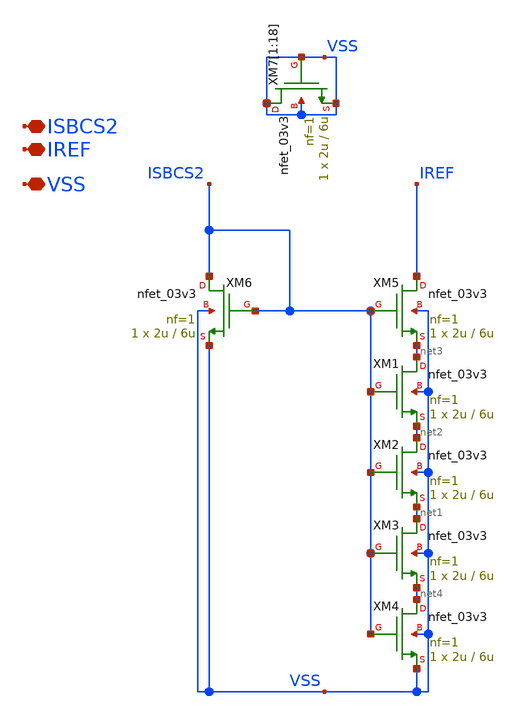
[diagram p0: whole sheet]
** sch_path: TIA_Filter/CurrentMirrors/CM_iref.sch
**.subckt CM_iref ISBCS2 IREF VSS
*.iopin ISBCS2
*.iopin IREF
*.iopin VSS
XM6 ISBCS2 ISBCS2 VSS VSS nfet_03v3 L=6u W=2u nf=1 ad='int((nf+1)/2) * W/nf * 0.18u' as='int((nf+2)/2) * W/nf * 0.18u'
+ pd='2*int((nf+1)/2) * (W/nf + 0.18u)' ps='2*int((nf+2)/2) * (W/nf + 0.18u)' nrd='0.18u / W' nrs='0.18u / W'
+ sa=0 sb=0 sd=0 m=1
XM5 IREF ISBCS2 net3 VSS nfet_03v3 L=6u W=2u nf=1 ad='int((nf+1)/2) * W/nf * 0.18u' as='int((nf+2)/2) * W/nf * 0.18u'
+ pd='2*int((nf+1)/2) * (W/nf + 0.18u)' ps='2*int((nf+2)/2) * (W/nf + 0.18u)' nrd='0.18u / W' nrs='0.18u / W'
+ sa=0 sb=0 sd=0 m=1
XM1 net3 ISBCS2 net2 VSS nfet_03v3 L=6u W=2u nf=1 ad='int((nf+1)/2) * W/nf * 0.18u' as='int((nf+2)/2) * W/nf * 0.18u'
+ pd='2*int((nf+1)/2) * (W/nf + 0.18u)' ps='2*int((nf+2)/2) * (W/nf + 0.18u)' nrd='0.18u / W' nrs='0.18u / W'
+ sa=0 sb=0 sd=0 m=1
XM2 net2 ISBCS2 net1 VSS nfet_03v3 L=6u W=2u nf=1 ad='int((nf+1)/2) * W/nf * 0.18u' as='int((nf+2)/2) * W/nf * 0.18u'
+ pd='2*int((nf+1)/2) * (W/nf + 0.18u)' ps='2*int((nf+2)/2) * (W/nf + 0.18u)' nrd='0.18u / W' nrs='0.18u / W'
+ sa=0 sb=0 sd=0 m=1
XM3 net1 ISBCS2 net4 VSS nfet_03v3 L=6u W=2u nf=1 ad='int((nf+1)/2) * W/nf * 0.18u' as='int((nf+2)/2) * W/nf * 0.18u'
+ pd='2*int((nf+1)/2) * (W/nf + 0.18u)' ps='2*int((nf+2)/2) * (W/nf + 0.18u)' nrd='0.18u / W' nrs='0.18u / W'
+ sa=0 sb=0 sd=0 m=1
XM4 net4 ISBCS2 VSS VSS nfet_03v3 L=6u W=2u nf=1 ad='int((nf+1)/2) * W/nf * 0.18u' as='int((nf+2)/2) * W/nf * 0.18u'
+ pd='2*int((nf+1)/2) * (W/nf + 0.18u)' ps='2*int((nf+2)/2) * (W/nf + 0.18u)' nrd='0.18u / W' nrs='0.18u / W'
+ sa=0 sb=0 sd=0 m=1
XM7[1] VSS VSS VSS VSS nfet_03v3 L=6u W=2u nf=1 ad='int((nf+1)/2) * W/nf * 0.18u' as='int((nf+2)/2) * W/nf * 0.18u'
+ pd='2*int((nf+1)/2) * (W/nf + 0.18u)' ps='2*int((nf+2)/2) * (W/nf + 0.18u)' nrd='0.18u / W' nrs='0.18u / W'
+ sa=0 sb=0 sd=0 m=1
XM7[2] VSS VSS VSS VSS nfet_03v3 L=6u W=2u nf=1 ad='int((nf+1)/2) * W/nf * 0.18u' as='int((nf+2)/2) * W/nf * 0.18u'
+ pd='2*int((nf+1)/2) * (W/nf + 0.18u)' ps='2*int((nf+2)/2) * (W/nf + 0.18u)' nrd='0.18u / W' nrs='0.18u / W'
+ sa=0 sb=0 sd=0 m=1
XM7[3] VSS VSS VSS VSS nfet_03v3 L=6u W=2u nf=1 ad='int((nf+1)/2) * W/nf * 0.18u' as='int((nf+2)/2) * W/nf * 0.18u'
+ pd='2*int((nf+1)/2) * (W/nf + 0.18u)' ps='2*int((nf+2)/2) * (W/nf + 0.18u)' nrd='0.18u / W' nrs='0.18u / W'
+ sa=0 sb=0 sd=0 m=1
XM7[4] VSS VSS VSS VSS nfet_03v3 L=6u W=2u nf=1 ad='int((nf+1)/2) * W/nf * 0.18u' as='int((nf+2)/2) * W/nf * 0.18u'
+ pd='2*int((nf+1)/2) * (W/nf + 0.18u)' ps='2*int((nf+2)/2) * (W/nf + 0.18u)' nrd='0.18u / W' nrs='0.18u / W'
+ sa=0 sb=0 sd=0 m=1
XM7[5] VSS VSS VSS VSS nfet_03v3 L=6u W=2u nf=1 ad='int((nf+1)/2) * W/nf * 0.18u' as='int((nf+2)/2) * W/nf * 0.18u'
+ pd='2*int((nf+1)/2) * (W/nf + 0.18u)' ps='2*int((nf+2)/2) * (W/nf + 0.18u)' nrd='0.18u / W' nrs='0.18u / W'
+ sa=0 sb=0 sd=0 m=1
XM7[6] VSS VSS VSS VSS nfet_03v3 L=6u W=2u nf=1 ad='int((nf+1)/2) * W/nf * 0.18u' as='int((nf+2)/2) * W/nf * 0.18u'
+ pd='2*int((nf+1)/2) * (W/nf + 0.18u)' ps='2*int((nf+2)/2) * (W/nf + 0.18u)' nrd='0.18u / W' nrs='0.18u / W'
+ sa=0 sb=0 sd=0 m=1
XM7[7] VSS VSS VSS VSS nfet_03v3 L=6u W=2u nf=1 ad='int((nf+1)/2) * W/nf * 0.18u' as='int((nf+2)/2) * W/nf * 0.18u'
+ pd='2*int((nf+1)/2) * (W/nf + 0.18u)' ps='2*int((nf+2)/2) * (W/nf + 0.18u)' nrd='0.18u / W' nrs='0.18u / W'
+ sa=0 sb=0 sd=0 m=1
XM7[8] VSS VSS VSS VSS nfet_03v3 L=6u W=2u nf=1 ad='int((nf+1)/2) * W/nf * 0.18u' as='int((nf+2)/2) * W/nf * 0.18u'
+ pd='2*int((nf+1)/2) * (W/nf + 0.18u)' ps='2*int((nf+2)/2) * (W/nf + 0.18u)' nrd='0.18u / W' nrs='0.18u / W'
+ sa=0 sb=0 sd=0 m=1
XM7[9] VSS VSS VSS VSS nfet_03v3 L=6u W=2u nf=1 ad='int((nf+1)/2) * W/nf * 0.18u' as='int((nf+2)/2) * W/nf * 0.18u'
+ pd='2*int((nf+1)/2) * (W/nf + 0.18u)' ps='2*int((nf+2)/2) * (W/nf + 0.18u)' nrd='0.18u / W' nrs='0.18u / W'
+ sa=0 sb=0 sd=0 m=1
XM7[10] VSS VSS VSS VSS nfet_03v3 L=6u W=2u nf=1 ad='int((nf+1)/2) * W/nf * 0.18u' as='int((nf+2)/2) * W/nf * 0.18u'
+ pd='2*int((nf+1)/2) * (W/nf + 0.18u)' ps='2*int((nf+2)/2) * (W/nf + 0.18u)' nrd='0.18u / W' nrs='0.18u / W'
+ sa=0 sb=0 sd=0 m=1
XM7[11] VSS VSS VSS VSS nfet_03v3 L=6u W=2u nf=1 ad='int((nf+1)/2) * W/nf * 0.18u' as='int((nf+2)/2) * W/nf * 0.18u'
+ pd='2*int((nf+1)/2) * (W/nf + 0.18u)' ps='2*int((nf+2)/2) * (W/nf + 0.18u)' nrd='0.18u / W' nrs='0.18u / W'
+ sa=0 sb=0 sd=0 m=1
XM7[12] VSS VSS VSS VSS nfet_03v3 L=6u W=2u nf=1 ad='int((nf+1)/2) * W/nf * 0.18u' as='int((nf+2)/2) * W/nf * 0.18u'
+ pd='2*int((nf+1)/2) * (W/nf + 0.18u)' ps='2*int((nf+2)/2) * (W/nf + 0.18u)' nrd='0.18u / W' nrs='0.18u / W'
+ sa=0 sb=0 sd=0 m=1
XM7[13] VSS VSS VSS VSS nfet_03v3 L=6u W=2u nf=1 ad='int((nf+1)/2) * W/nf * 0.18u' as='int((nf+2)/2) * W/nf * 0.18u'
+ pd='2*int((nf+1)/2) * (W/nf + 0.18u)' ps='2*int((nf+2)/2) * (W/nf + 0.18u)' nrd='0.18u / W' nrs='0.18u / W'
+ sa=0 sb=0 sd=0 m=1
XM7[14] VSS VSS VSS VSS nfet_03v3 L=6u W=2u nf=1 ad='int((nf+1)/2) * W/nf * 0.18u' as='int((nf+2)/2) * W/nf * 0.18u'
+ pd='2*int((nf+1)/2) * (W/nf + 0.18u)' ps='2*int((nf+2)/2) * (W/nf + 0.18u)' nrd='0.18u / W' nrs='0.18u / W'
+ sa=0 sb=0 sd=0 m=1
XM7[15] VSS VSS VSS VSS nfet_03v3 L=6u W=2u nf=1 ad='int((nf+1)/2) * W/nf * 0.18u' as='int((nf+2)/2) * W/nf * 0.18u'
+ pd='2*int((nf+1)/2) * (W/nf + 0.18u)' ps='2*int((nf+2)/2) * (W/nf + 0.18u)' nrd='0.18u / W' nrs='0.18u / W'
+ sa=0 sb=0 sd=0 m=1
XM7[16] VSS VSS VSS VSS nfet_03v3 L=6u W=2u nf=1 ad='int((nf+1)/2) * W/nf * 0.18u' as='int((nf+2)/2) * W/nf * 0.18u'
+ pd='2*int((nf+1)/2) * (W/nf + 0.18u)' ps='2*int((nf+2)/2) * (W/nf + 0.18u)' nrd='0.18u / W' nrs='0.18u / W'
+ sa=0 sb=0 sd=0 m=1
XM7[17] VSS VSS VSS VSS nfet_03v3 L=6u W=2u nf=1 ad='int((nf+1)/2) * W/nf * 0.18u' as='int((nf+2)/2) * W/nf * 0.18u'
+ pd='2*int((nf+1)/2) * (W/nf + 0.18u)' ps='2*int((nf+2)/2) * (W/nf + 0.18u)' nrd='0.18u / W' nrs='0.18u / W'
+ sa=0 sb=0 sd=0 m=1
XM7[18] VSS VSS VSS VSS nfet_03v3 L=6u W=2u nf=1 ad='int((nf+1)/2) * W/nf * 0.18u' as='int((nf+2)/2) * W/nf * 0.18u'
+ pd='2*int((nf+1)/2) * (W/nf + 0.18u)' ps='2*int((nf+2)/2) * (W/nf + 0.18u)' nrd='0.18u / W' nrs='0.18u / W'
+ sa=0 sb=0 sd=0 m=1
**.ends
.end
